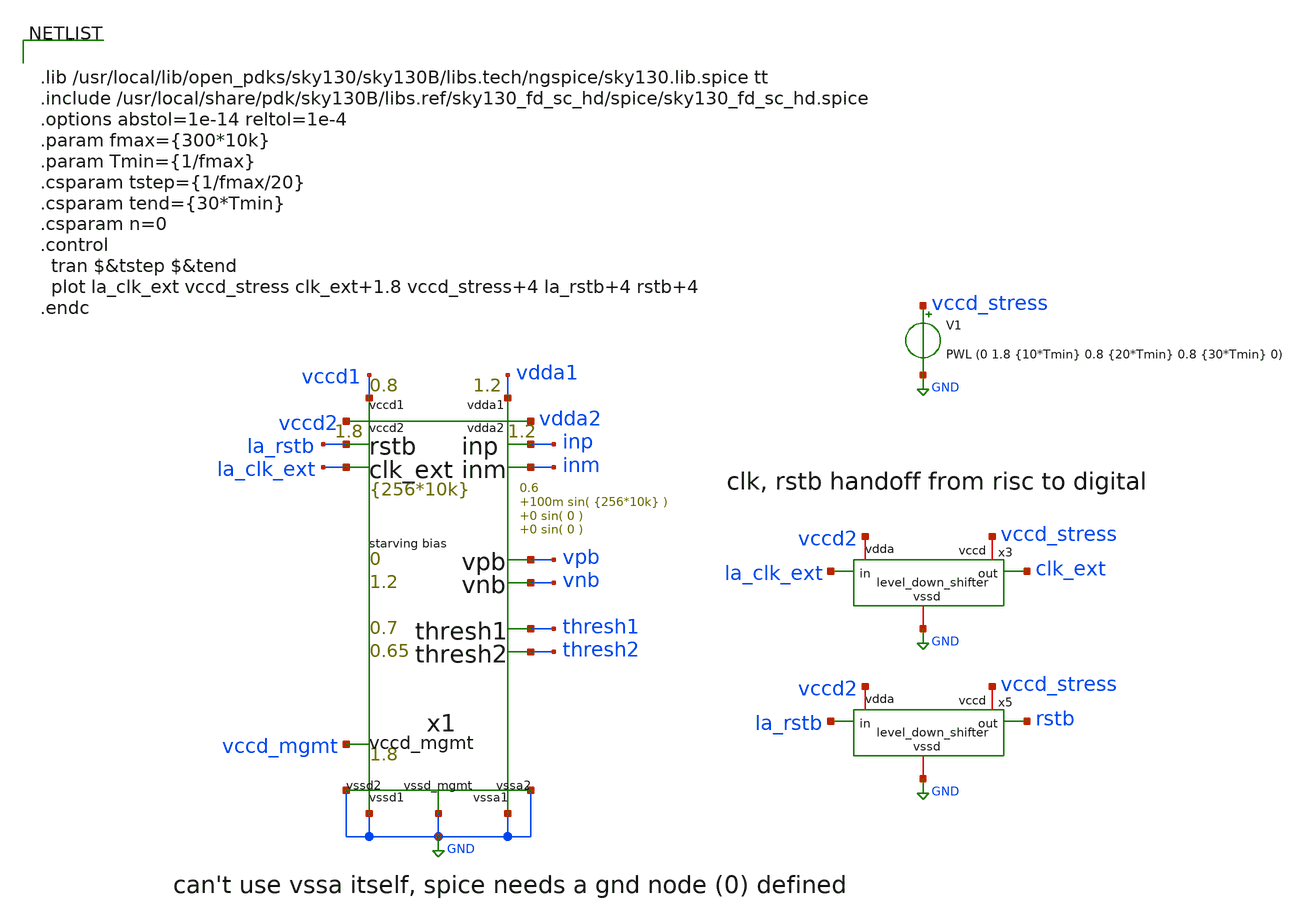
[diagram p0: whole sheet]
** sch_path: xschem/test_bench/level_down_shifter_stress.sch
**.subckt level_down_shifter_stress
x1 thresh1 thresh2 vdda1 GND inp inm la_clk_ext la_rstb vccd1 GND vpb vnb vccd_mgmt GND vccd2 vdda2 GND
+ GND pad_frame p_vdda1=1.2 p_vdda2=1.2 p_vccd1=0.8 p_vccd2=1.8 p_vccd_mgmt=1.8 p_fclk={256*10k} p_duty_cycle=0.5
+ p_rstb_delay={1.5/p_fclk} p_rstb_tr=5n p_thresh1=0.7 p_thresh2=0.65 p_vpb=0 p_vnb=1.2 p_vcm=0.6 p_amp1=100m
+ p_f1={256*10k} p_amp2=0 p_f2=0 p_amp3=0 p_f3=0
x3 vccd2 vccd_stress la_clk_ext clk_ext GND level_down_shifter
x5 vccd2 vccd_stress la_rstb rstb GND level_down_shifter
V1 vccd_stress GND PWL (0 1.8 {10*Tmin} 0.8 {20*Tmin} 0.8 {30*Tmin} 0)
**** begin user architecture code


.lib /usr/local/lib/open_pdks/sky130/sky130B/libs.tech/ngspice/sky130.lib.spice tt
.include /usr/local/share/pdk/sky130B/libs.ref/sky130_fd_sc_hd/spice/sky130_fd_sc_hd.spice
.options abstol=1e-14 reltol=1e-4
.param fmax={300*10k}
.param Tmin={1/fmax}
.csparam tstep={1/fmax/20}
.csparam tend={30*Tmin}
.csparam n=0
.control
  tran $&tstep $&tend
  plot la_clk_ext vccd_stress clk_ext+1.8 vccd_stress+4 la_rstb+4 rstb+4
.endc


**** end user architecture code
**.ends

* expanding   symbol:  test_bench/pad_frame.sym # of pins=18
** sym_path: xschem/test_bench/pad_frame.sym
** sch_path: xschem/test_bench/pad_frame.sch
.subckt pad_frame thresh1 thresh2 vdda1 vssa1 inp inm clk_ext rstb vccd1 vssd1 vpb vnb vccd_mgmt vssd_mgmt
+ vccd2 vdda2 vssd2 vssa2   p_vdda1=1.2  p_vdda2=1.2  p_vccd1=1  p_vccd2=1.8  p_vccd_mgmt=1.8  p_fclk={256*10k}
+  p_duty_cycle=0.5  p_rstb_delay={1.5/p_fclk}  p_rstb_tr=5n  p_thresh1=0.7  p_thresh2=0.65  p_vpb=0  p_vnb=1.2
+  p_vcm=0.6  p_amp1=100m  p_f1={256*10k}  p_amp2=0  p_f2=0  p_amp3=0  p_f3=0
*.opin thresh1
*.opin thresh2
*.opin inp
*.opin inm
*.opin rstb
*.opin clk_ext
*.opin vpb
*.opin vnb
*.iopin vccd1
*.iopin vssd1
*.iopin vdda1
*.iopin vssa1
*.iopin vdda2
*.iopin vssa2
*.iopin vccd2
*.iopin vssd2
*.iopin vccd_mgmt
*.iopin vssd_mgmt
vdda1 vdda1 vssa1 DC {p_vdda1}
vthresh1 thresh1 vssa1 DC {p_thresh1}
vthresh2 thresh2 vssa1 DC {p_thresh2}
vinp1 inp inp2 DC 0 SIN(0 {p_amp1} {p_f1})
vinm1 inm inm2 DC 0 SIN(0 {-p_amp1} {p_f1})
vpb vpb vssa1 DC {p_vpb}
vnb vnb vssa1 DC {p_vnb}
vinp2 inp2 inp3 DC 0 SIN(0 {p_amp2} {p_f2})
vinp3 inp3 vcm DC 0 SIN(0 {p_amp3} {p_f3})
vinm2 inm2 inm3 DC 0 SIN(0 {-p_amp2} {p_f2})
vinm3 inm3 vcm DC 0 SIN(0 {-p_amp3} {p_f3})
vcm vcm vssa1 DC {p_vcm}
vccd1 vccd1 vssd1 DC {p_vccd1}
Vclk clk vssd_mgmt DC 0 PULSE (0 p_vccd_mgmt 1n 1n 1n {p_duty_cycle*1/p_fclk} {1/p_fclk} 0
Vrstb rstb vssd_mgmt DC 0 PWL ( 0 0 p_rstb_delay 0 {p_rstb_delay + p_rstb_tr} p_vccd_mgmt)
x1 clk rstb vssd_mgmt vssd_mgmt vccd_mgmt vccd_mgmt clk_ext sky130_fd_sc_hd__dlclkp_1
vccd_mgmt vccd_mgmt vssd_mgmt DC {p_vccd_mgmt}
vccd2 vccd2 vssd2 DC {p_vccd2}
vdda5 vdda2 vssa2 DC {p_vdda2}
.ends


* expanding   symbol:  level_shifter/level_down_shifter.sym # of pins=5
** sym_path: xschem/level_shifter/level_down_shifter.sym
** sch_path: xschem/level_shifter/level_down_shifter.sch
.subckt level_down_shifter vdda vccd in out vssd
*.ipin in
*.iopin vssd
*.iopin vdda
*.opin out
*.iopin vccd
x1 in vssd vssd vdda vdda net1 sky130_fd_sc_hd__inv_8
x2 net1 vssd vssd vccd vccd out sky130_fd_sc_hd__inv_8
.ends

.GLOBAL GND
.end
